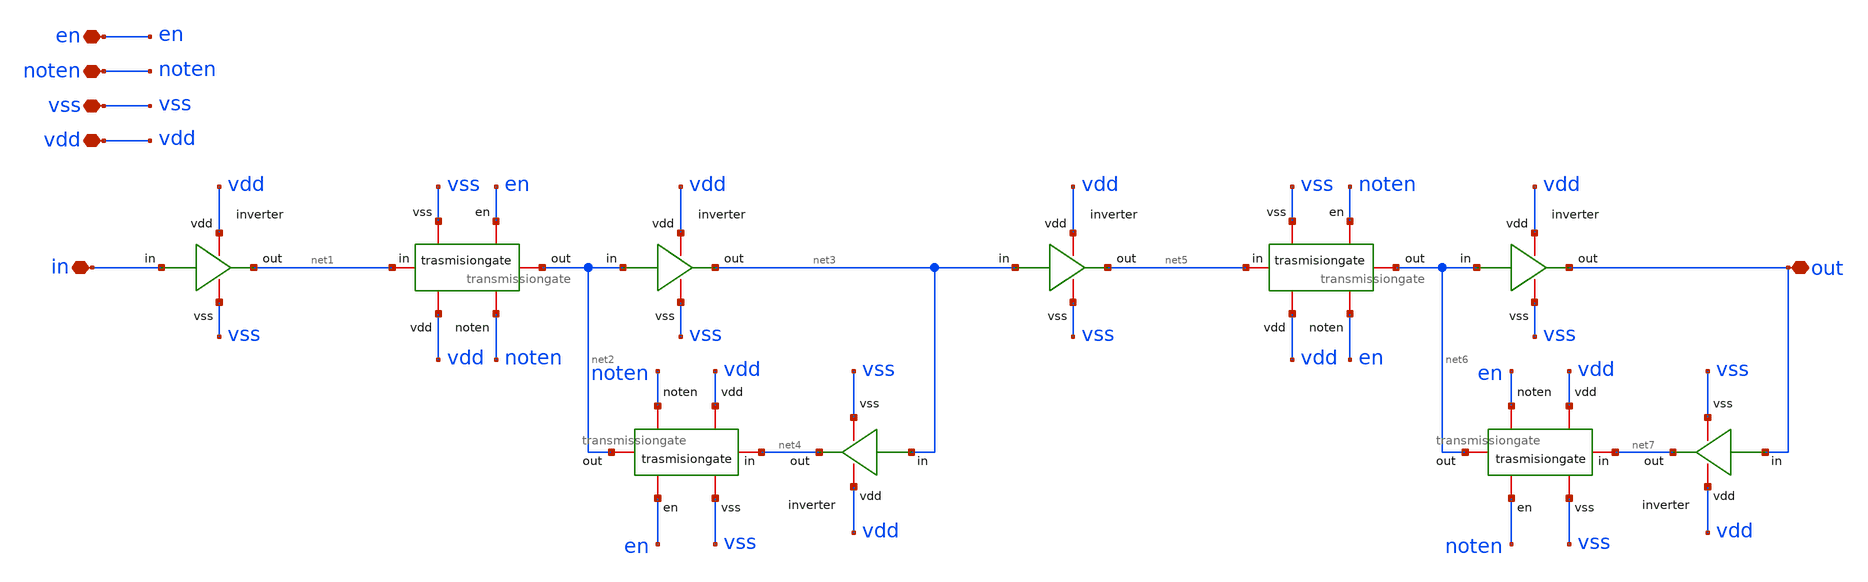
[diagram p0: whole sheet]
** sch_path: design/blocks/register/schematic/register.sch
**.subckt register in vdd vss out en noten
*.iopin in
*.iopin vdd
*.iopin vss
*.iopin out
*.iopin en
*.iopin noten
x1 vdd net1 in vss inverter
x3 vdd net3 net2 vss inverter
x4 vdd net4 net3 vss inverter
x5 net1 vdd noten net2 vss en transmissiongate
x6 net4 vdd noten net2 vss en transmissiongate
x7 vdd net5 net3 vss inverter
x9 vdd out net6 vss inverter
x10 vdd net7 out vss inverter
x11 net5 vdd en net6 vss noten transmissiongate
x12 net7 vdd en net6 vss noten transmissiongate
**.ends

* expanding   symbol:  blocks/inverter/schematic/inverter.sym # of pins=4
** sym_path: design/blocks/inverter/schematic/inverter.sym
** sch_path: design/blocks/inverter/schematic/inverter.sch
.subckt inverter vdd out in vss
*.iopin vdd
*.iopin out
*.iopin vss
*.iopin in
XM1 out in vss vss sg13_lv_nmos w=0.75u l=0.15u ng=1 m=1 mm_ok=1
XM2 out in vdd vdd sg13_lv_pmos w=1.5u l=0.15u ng=1 m=1 mm_ok=1
.ends


* expanding   symbol:  blocks/transmissiongate/schematic/transmissiongate.sym # of pins=6
** sym_path: design/blocks/transmissiongate/schematic/transmissiongate.sym
** sch_path: design/blocks/transmissiongate/schematic/transmissiongate.sch
.subckt transmissiongate in vdd noten out vss en
*.iopin noten
*.iopin en
*.iopin in
*.iopin out
*.iopin vdd
*.iopin vss
XM1 out noten in vdd sg13_lv_pmos w=1.5u l=0.15u ng=1 m=1 mm_ok=1
XM2 out en in vss sg13_lv_nmos w=0.75u l=0.15u ng=1 m=1 mm_ok=1
.ends

.end
